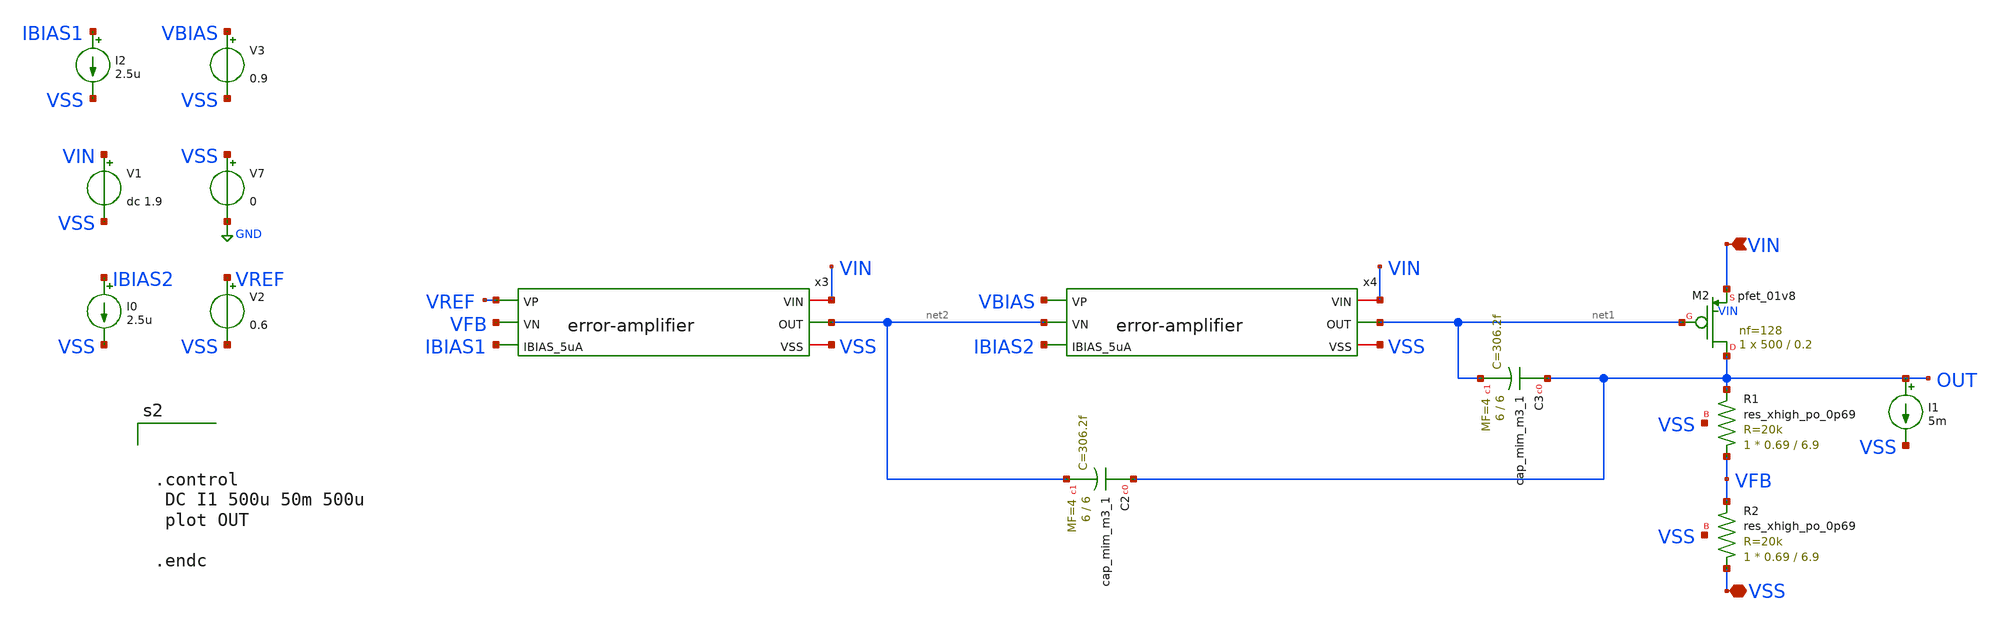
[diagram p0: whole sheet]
** sch_path: xschem/ldo_andriansyah/testbench/load-line-regulation.sch
**.subckt load-line-regulation VIN VSS
*.ipin VIN
*.iopin VSS
V7 VSS GND 0
V1 VIN VSS dc 1.9
V2 VREF VSS 0.6
I0 IBIAS2 VSS 2.5u
V3 VBIAS VSS 0.9
I2 IBIAS1 VSS 2.5u
I1 OUT VSS 5m
XC2 OUT net2 sky130_fd_pr__cap_mim_m3_1 W=6 L=6 MF=4 m=4
XC3 OUT net1 sky130_fd_pr__cap_mim_m3_1 W=6 L=6 MF=4 m=4
x3 VIN VREF VFB IBIAS1 net2 VSS error-amplifier
XR1 VFB OUT VSS sky130_fd_pr__res_xhigh_po_0p69 L=6.9 mult=1 m=1
XR2 VSS VFB VSS sky130_fd_pr__res_xhigh_po_0p69 L=6.9 mult=1 m=1
XM2 OUT net1 VIN VIN sky130_fd_pr__pfet_01v8 L=0.2 W=500 nf=128 ad='int((nf+1)/2) * W/nf * 0.29' as='int((nf+2)/2) * W/nf * 0.29'
+ pd='2*int((nf+1)/2) * (W/nf + 0.29)' ps='2*int((nf+2)/2) * (W/nf + 0.29)' nrd='0.29 / W' nrs='0.29 / W'
+ sa=0 sb=0 sd=0 mult=1 m=1
x4 VIN VBIAS net2 IBIAS2 net1 VSS error-amplifier
**** begin user architecture code

** opencircuitdesign pdks install
.lib $::SKYWATER_MODELS/sky130.lib.spice tt





.control
 DC I1 500u 50m 500u
 plot OUT

.endc




**** end user architecture code
**.ends

* expanding   symbol:
*+  /foss/designs/2026/tt_sky26b_ldo_andriansyah/xschem/error-amplifier/error-amplifier.sym # of pins=6
** sym_path: xschem/error-amplifier/error-amplifier.sym
** sch_path: xschem/error-amplifier/error-amplifier.sch
.subckt error-amplifier VIN VP VN IBIAS_5uA OUT VSS
*.ipin IBIAS_5uA
*.ipin VN
*.ipin VP
*.iopin VIN
*.iopin VSS
*.opin OUT
XM1 net2 net2 VSS VSS sky130_fd_pr__nfet_01v8 L=0.6 W=4.2 nf=4 ad='int((nf+1)/2) * W/nf * 0.29' as='int((nf+2)/2) * W/nf * 0.29'
+ pd='2*int((nf+1)/2) * (W/nf + 0.29)' ps='2*int((nf+2)/2) * (W/nf + 0.29)' nrd='0.29 / W' nrs='0.29 / W'
+ sa=0 sb=0 sd=0 mult=1 m=1
XM2 OUT net2 VSS VSS sky130_fd_pr__nfet_01v8 L=0.6 W=4.2 nf=4 ad='int((nf+1)/2) * W/nf * 0.29' as='int((nf+2)/2) * W/nf * 0.29'
+ pd='2*int((nf+1)/2) * (W/nf + 0.29)' ps='2*int((nf+2)/2) * (W/nf + 0.29)' nrd='0.29 / W' nrs='0.29 / W'
+ sa=0 sb=0 sd=0 mult=1 m=1
XM3 net2 VN net1 VDD sky130_fd_pr__pfet_01v8 L=0.6 W=28 nf=4 ad='int((nf+1)/2) * W/nf * 0.29' as='int((nf+2)/2) * W/nf * 0.29'
+ pd='2*int((nf+1)/2) * (W/nf + 0.29)' ps='2*int((nf+2)/2) * (W/nf + 0.29)' nrd='0.29 / W' nrs='0.29 / W'
+ sa=0 sb=0 sd=0 mult=1 m=1
XM4 OUT VP net1 VDD sky130_fd_pr__pfet_01v8 L=0.6 W=28 nf=4 ad='int((nf+1)/2) * W/nf * 0.29' as='int((nf+2)/2) * W/nf * 0.29'
+ pd='2*int((nf+1)/2) * (W/nf + 0.29)' ps='2*int((nf+2)/2) * (W/nf + 0.29)' nrd='0.29 / W' nrs='0.29 / W'
+ sa=0 sb=0 sd=0 mult=1 m=1
XM5 net1 IBIAS_5uA VIN VIN sky130_fd_pr__pfet_01v8 L=0.6 W=6.6 nf=4 ad='int((nf+1)/2) * W/nf * 0.29'
+ as='int((nf+2)/2) * W/nf * 0.29' pd='2*int((nf+1)/2) * (W/nf + 0.29)' ps='2*int((nf+2)/2) * (W/nf + 0.29)'
+ nrd='0.29 / W' nrs='0.29 / W' sa=0 sb=0 sd=0 mult=1 m=1
XM6 IBIAS_5uA IBIAS_5uA VIN VIN sky130_fd_pr__pfet_01v8 L=0.6 W=6.6 nf=4 ad='int((nf+1)/2) * W/nf * 0.29'
+ as='int((nf+2)/2) * W/nf * 0.29' pd='2*int((nf+1)/2) * (W/nf + 0.29)' ps='2*int((nf+2)/2) * (W/nf + 0.29)'
+ nrd='0.29 / W' nrs='0.29 / W' sa=0 sb=0 sd=0 mult=1 m=1
XM7 VDD VDD VDD VDD sky130_fd_pr__pfet_01v8 L=0.6 W=7 nf=1 ad='int((nf+1)/2) * W/nf * 0.29' as='int((nf+2)/2) * W/nf * 0.29'
+ pd='2*int((nf+1)/2) * (W/nf + 0.29)' ps='2*int((nf+2)/2) * (W/nf + 0.29)' nrd='0.29 / W' nrs='0.29 / W'
+ sa=0 sb=0 sd=0 mult=1 m=1
XM8 VSS VSS VSS VSS sky130_fd_pr__nfet_01v8 L=0.6 W=1.05 nf=1 ad='int((nf+1)/2) * W/nf * 0.29' as='int((nf+2)/2) * W/nf * 0.29'
+ pd='2*int((nf+1)/2) * (W/nf + 0.29)' ps='2*int((nf+2)/2) * (W/nf + 0.29)' nrd='0.29 / W' nrs='0.29 / W'
+ sa=0 sb=0 sd=0 mult=1 m=1
XM9 VDD VDD VDD VDD sky130_fd_pr__pfet_01v8 L=0.6 W=1.65 nf=1 ad='int((nf+1)/2) * W/nf * 0.29' as='int((nf+2)/2) * W/nf * 0.29'
+ pd='2*int((nf+1)/2) * (W/nf + 0.29)' ps='2*int((nf+2)/2) * (W/nf + 0.29)' nrd='0.29 / W' nrs='0.29 / W'
+ sa=0 sb=0 sd=0 mult=1 m=1
XM10 VSS VSS VSS VSS sky130_fd_pr__nfet_01v8 L=0.6 W=1.05 nf=1 ad='int((nf+1)/2) * W/nf * 0.29' as='int((nf+2)/2) * W/nf * 0.29'
+ pd='2*int((nf+1)/2) * (W/nf + 0.29)' ps='2*int((nf+2)/2) * (W/nf + 0.29)' nrd='0.29 / W' nrs='0.29 / W'
+ sa=0 sb=0 sd=0 mult=1 m=1
XM11 VDD VDD VDD VDD sky130_fd_pr__pfet_01v8 L=0.6 W=7 nf=1 ad='int((nf+1)/2) * W/nf * 0.29' as='int((nf+2)/2) * W/nf * 0.29'
+ pd='2*int((nf+1)/2) * (W/nf + 0.29)' ps='2*int((nf+2)/2) * (W/nf + 0.29)' nrd='0.29 / W' nrs='0.29 / W'
+ sa=0 sb=0 sd=0 mult=1 m=1
XM12 VDD VDD VDD VDD sky130_fd_pr__pfet_01v8 L=0.6 W=1.65 nf=1 ad='int((nf+1)/2) * W/nf * 0.29' as='int((nf+2)/2) * W/nf * 0.29'
+ pd='2*int((nf+1)/2) * (W/nf + 0.29)' ps='2*int((nf+2)/2) * (W/nf + 0.29)' nrd='0.29 / W' nrs='0.29 / W'
+ sa=0 sb=0 sd=0 mult=1 m=1
.ends

.GLOBAL GND
.end
